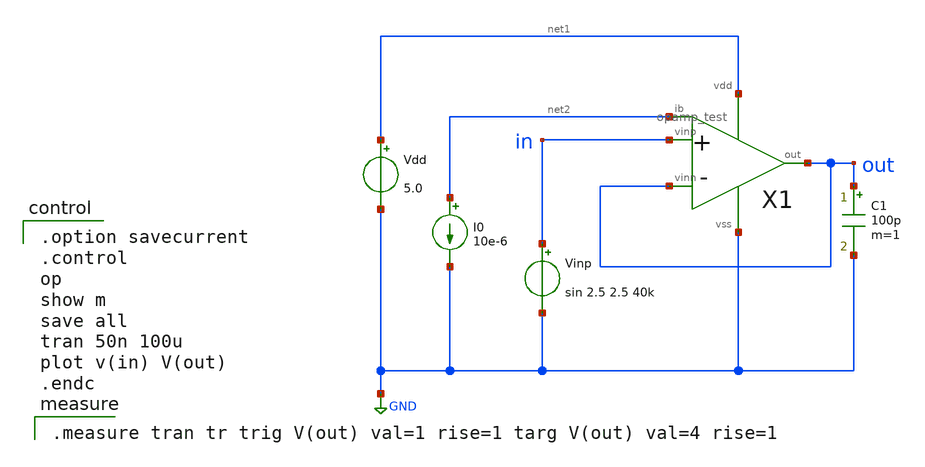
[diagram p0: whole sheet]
** sch_path: member_project/opamp/cat_nekonekone/opamp_tran.sch
**.subckt opamp_tran
Vdd net1 GND 5.0
C1 out GND 100p m=1
I0 net2 GND 10e-6
Vinp in GND sin 2.5 2.5 40k
X1 in out net2 out net1 GND opamp_test
**** begin user architecture code

.option savecurrent
.control
op
show m
save all
tran 50n 100u
plot v(in) V(out)
.endc


.measure tran tr trig V(out) val=1 rise=1 targ V(out) val=4 rise=1

 .include $::LIB/ip62_models
**** end user architecture code
**.ends

* expanding   symbol:  opamp_test.sym # of pins=6
** sym_path: member_project/opamp/cat_nekonekone/opamp_test.sym
** sch_path: member_project/opamp/cat_nekonekone/opamp_test.sch
.subckt opamp_test vinp vinn ib out vdd vss
*.ipin vinn
*.ipin vinp
*.opin out
*.iopin ib
*.iopin vss
*.iopin vdd
XXM1 net2 vinn net1 vdd PMOS w=25u l=5u nrd=0 nrs=0 m=12
XXM4 net3 net2 vss vss NMOS w=25u l=5u nrd=0 nrs=0 m=8
XXM2 net3 vinp net1 vdd PMOS w=25u l=5u nrd=0 nrs=0 m=12
XXM3 net2 net2 vss vss NMOS w=25u l=5u nrd=0 nrs=0 m=8
XXM5 net1 ib vdd vdd PMOS w=25u l=5u nrd=0 nrs=0 m=16
XXM6 out ib vdd vdd PMOS w=25u l=5u nrd=0 nrs=0 m=32
XXM7 out net3 vss vss NMOS w=25u l=5u nrd=0 nrs=0 m=34
XXM8 ib ib vdd vdd PMOS w=25u l=5u nrd=0 nrs=0 m=1
XXM9 net5 ib vdd vdd PMOS w=25u l=5u nrd=0 nrs=0 m=2
XXM10 net5 net5 net4 vss NMOS w=25u l=5u nrd=0 nrs=0 m=2
XXM11 net4 net4 vss vss NMOS w=25u l=5u nrd=0 nrs=0 m=2
XXM12 net6 net5 net3 vss NMOS w=25u l=5u nrd=0 nrs=0 m=4
XXM_DUMMY2 vdd vdd vdd vdd PMOS w=25u l=5u nrd=0 nrs=0 m=4
XXM_DUMMY1 vss vss vss vss NMOS w=25u l=5u nrd=0 nrs=0 m=24
XXM_DUMMY3 net1 vdd vdd vdd PMOS w=25u l=5u nrd=0 nrs=0 m=4
XXM_DUMMY5 net3 vss vss vss NMOS w=25u l=5u nrd=0 nrs=0 m=2
XXM_DUMMY4 net5 vdd vdd vdd PMOS w=25u l=5u nrd=0 nrs=0 m=2
XXM_DUMMY6 ib vdd vdd vdd PMOS w=25u l=5u nrd=0 nrs=0 m=1
XXM_DUMMY7 out vss vss vss NMOS w=25u l=5u nrd=0 nrs=0 m=2
XXC2 net6 out vss F_CSIO c=4.954p x=96u y=86u m=4
.ends

.GLOBAL GND
.end
